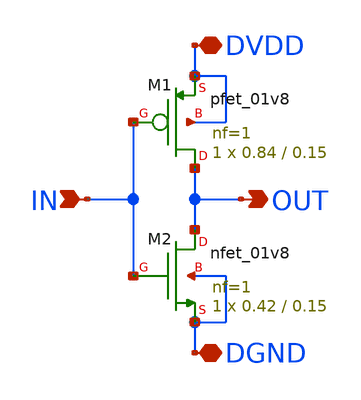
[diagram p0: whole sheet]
** sch_path: tut5/inv/cell/primitive/inv.sch
**.subckt inv DVDD DGND OUT IN
*.iopin DVDD
*.iopin DGND
*.opin OUT
*.ipin IN
XM1 OUT IN DVDD DVDD sky130_fd_pr__pfet_01v8 L=0.15 W=0.84 nf=1 ad='int((nf+1)/2) * W/nf * 0.29' as='int((nf+2)/2) * W/nf * 0.29'
+ pd='2*int((nf+1)/2) * (W/nf + 0.29)' ps='2*int((nf+2)/2) * (W/nf + 0.29)' nrd='0.29 / W' nrs='0.29 / W'
+ sa=0 sb=0 sd=0 mult=1 m=1
XM2 OUT IN DGND DGND sky130_fd_pr__nfet_01v8 L=0.15 W=0.42 nf=1 ad='int((nf+1)/2) * W/nf * 0.29' as='int((nf+2)/2) * W/nf * 0.29'
+ pd='2*int((nf+1)/2) * (W/nf + 0.29)' ps='2*int((nf+2)/2) * (W/nf + 0.29)' nrd='0.29 / W' nrs='0.29 / W'
+ sa=0 sb=0 sd=0 mult=1 m=1
**.ends
.end
